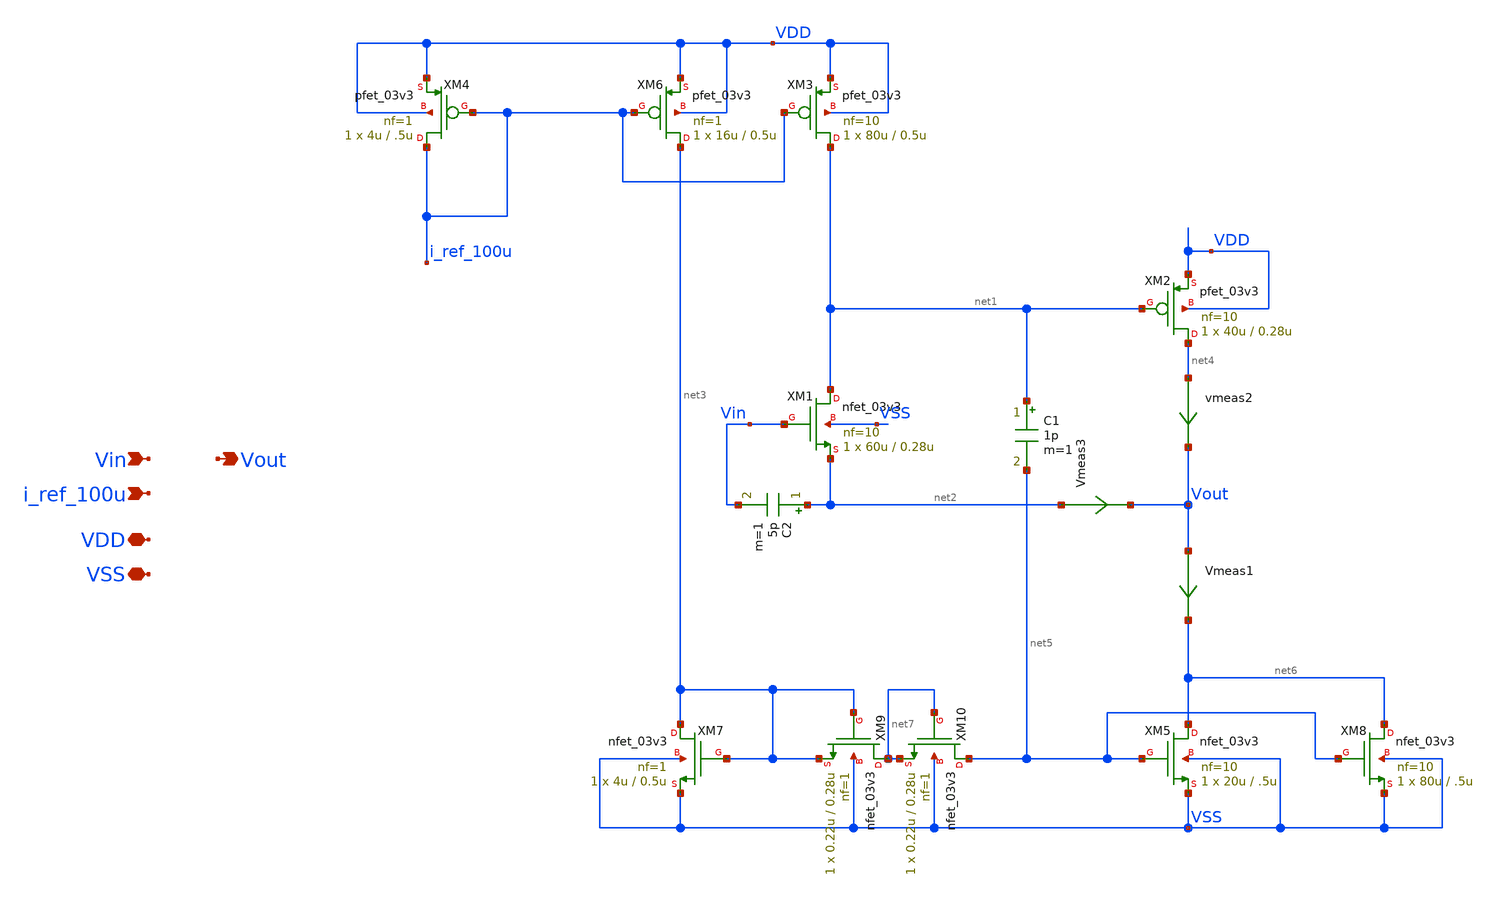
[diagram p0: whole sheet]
** sch_path: designs/output_buffer/schematic/output_buffer.sch
**.subckt output_buffer Vin Vout i_ref_100u VDD VSS
*.ipin Vin
*.opin Vout
*.ipin i_ref_100u
*.iopin VDD
*.iopin VSS
XM1 net1 Vin net2 VSS nfet_03v3 L=0.28u W=60u nf=10 ad='int((nf+1)/2) * W/nf * 0.18u' as='int((nf+2)/2) * W/nf * 0.18u'
+ pd='2*int((nf+1)/2) * (W/nf + 0.18u)' ps='2*int((nf+2)/2) * (W/nf + 0.18u)' nrd='0.18u / W' nrs='0.18u / W'
+ sa=0 sb=0 sd=0 m=1
XM2 net4 net1 VDD VDD pfet_03v3 L=0.28u W=40u nf=10 ad='int((nf+1)/2) * W/nf * 0.18u' as='int((nf+2)/2) * W/nf * 0.18u'
+ pd='2*int((nf+1)/2) * (W/nf + 0.18u)' ps='2*int((nf+2)/2) * (W/nf + 0.18u)' nrd='0.18u / W' nrs='0.18u / W'
+ sa=0 sb=0 sd=0 m=1
XM3 net1 i_ref_100u VDD VDD pfet_03v3 L=0.5u W=80u nf=10 ad='int((nf+1)/2) * W/nf * 0.18u' as='int((nf+2)/2) * W/nf * 0.18u'
+ pd='2*int((nf+1)/2) * (W/nf + 0.18u)' ps='2*int((nf+2)/2) * (W/nf + 0.18u)' nrd='0.18u / W' nrs='0.18u / W'
+ sa=0 sb=0 sd=0 m=1
XM4 i_ref_100u i_ref_100u VDD VDD pfet_03v3 L=.5u W=4u nf=1 ad='int((nf+1)/2) * W/nf * 0.18u' as='int((nf+2)/2) * W/nf * 0.18u'
+ pd='2*int((nf+1)/2) * (W/nf + 0.18u)' ps='2*int((nf+2)/2) * (W/nf + 0.18u)' nrd='0.18u / W' nrs='0.18u / W'
+ sa=0 sb=0 sd=0 m=1
XM5 net6 net5 VSS VSS nfet_03v3 L=.5u W=20u nf=10 ad='int((nf+1)/2) * W/nf * 0.18u' as='int((nf+2)/2) * W/nf * 0.18u'
+ pd='2*int((nf+1)/2) * (W/nf + 0.18u)' ps='2*int((nf+2)/2) * (W/nf + 0.18u)' nrd='0.18u / W' nrs='0.18u / W'
+ sa=0 sb=0 sd=0 m=1
vmeas2 net4 Vout 0
.save i(vmeas2)
Vmeas1 Vout net6 0
.save i(vmeas1)
C1 net1 net5 1p m=1
XM6 net3 i_ref_100u VDD VDD pfet_03v3 L=0.5u W=16u nf=1 ad='int((nf+1)/2) * W/nf * 0.18u' as='int((nf+2)/2) * W/nf * 0.18u'
+ pd='2*int((nf+1)/2) * (W/nf + 0.18u)' ps='2*int((nf+2)/2) * (W/nf + 0.18u)' nrd='0.18u / W' nrs='0.18u / W'
+ sa=0 sb=0 sd=0 m=1
XM7 net3 net3 VSS VSS nfet_03v3 L=0.5u W=4u nf=1 ad='int((nf+1)/2) * W/nf * 0.18u' as='int((nf+2)/2) * W/nf * 0.18u'
+ pd='2*int((nf+1)/2) * (W/nf + 0.18u)' ps='2*int((nf+2)/2) * (W/nf + 0.18u)' nrd='0.18u / W' nrs='0.18u / W'
+ sa=0 sb=0 sd=0 m=1
Vmeas3 net2 Vout 0
.save i(vmeas3)
XM8 net6 net5 VSS VSS nfet_03v3 L=.5u W=80u nf=10 ad='int((nf+1)/2) * W/nf * 0.18u' as='int((nf+2)/2) * W/nf * 0.18u'
+ pd='2*int((nf+1)/2) * (W/nf + 0.18u)' ps='2*int((nf+2)/2) * (W/nf + 0.18u)' nrd='0.18u / W' nrs='0.18u / W'
+ sa=0 sb=0 sd=0 m=1
XM9 net7 net3 net3 VSS nfet_03v3 L=0.28u W=0.22u nf=1 ad='int((nf+1)/2) * W/nf * 0.18u' as='int((nf+2)/2) * W/nf * 0.18u'
+ pd='2*int((nf+1)/2) * (W/nf + 0.18u)' ps='2*int((nf+2)/2) * (W/nf + 0.18u)' nrd='0.18u / W' nrs='0.18u / W'
+ sa=0 sb=0 sd=0 m=1
XM10 net5 net7 net7 VSS nfet_03v3 L=0.28u W=0.22u nf=1 ad='int((nf+1)/2) * W/nf * 0.18u' as='int((nf+2)/2) * W/nf * 0.18u'
+ pd='2*int((nf+1)/2) * (W/nf + 0.18u)' ps='2*int((nf+2)/2) * (W/nf + 0.18u)' nrd='0.18u / W' nrs='0.18u / W'
+ sa=0 sb=0 sd=0 m=1
C2 net2 Vin 5p m=1
**.ends
.end
